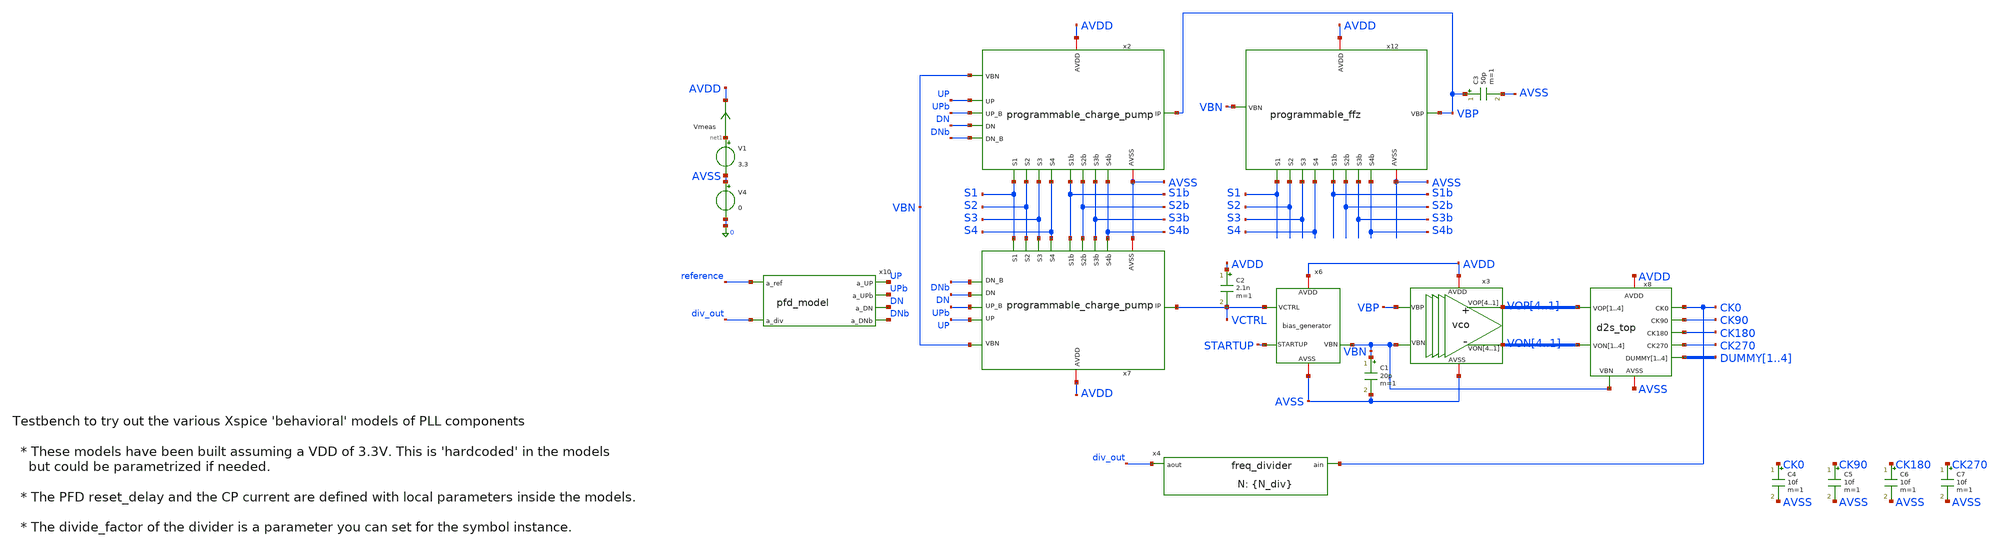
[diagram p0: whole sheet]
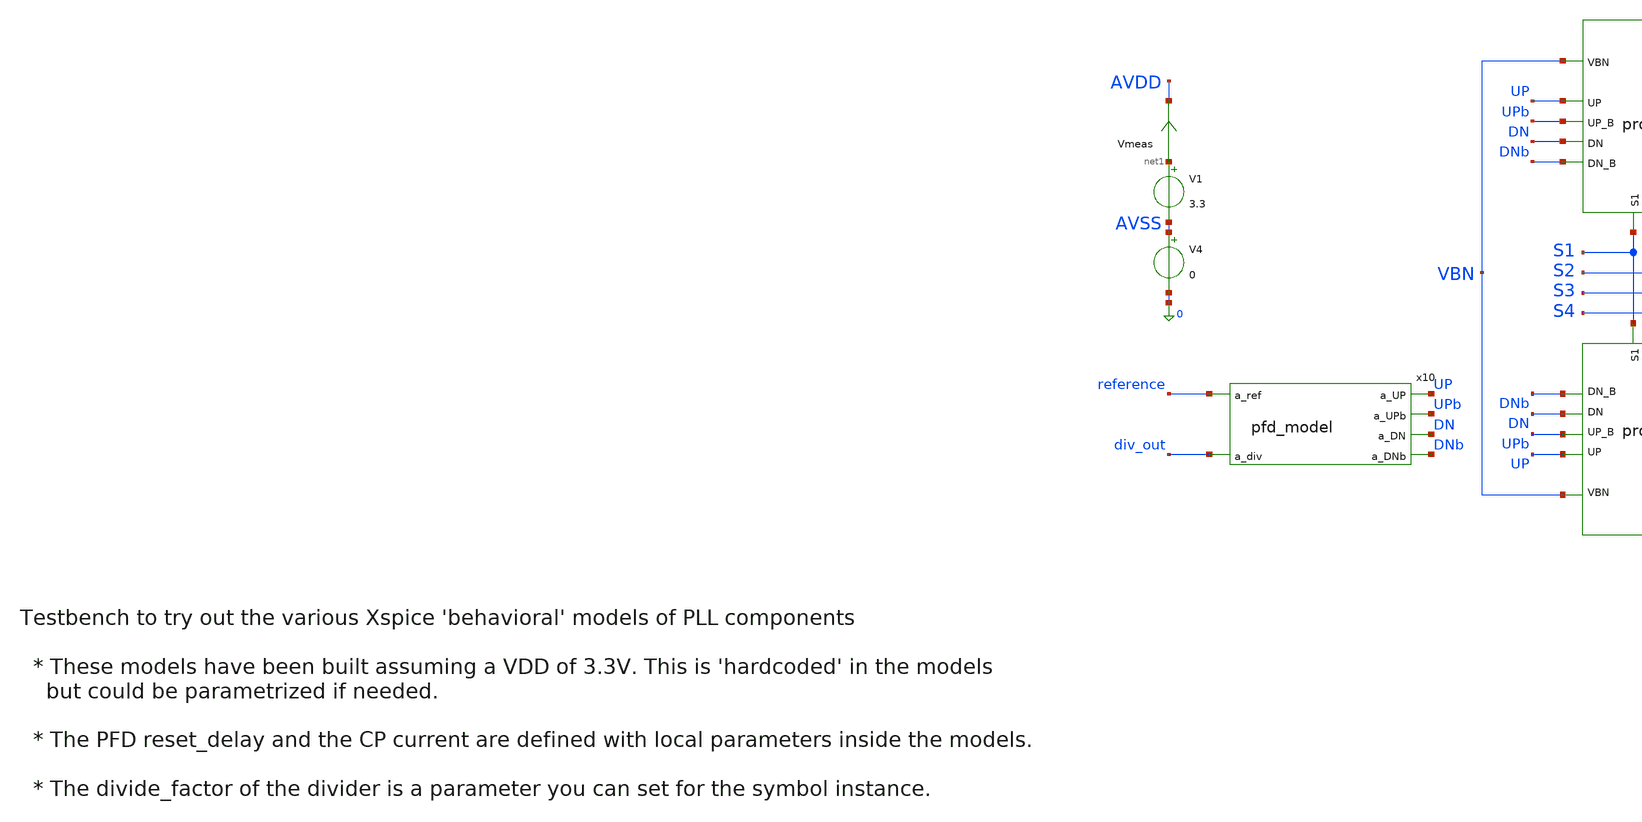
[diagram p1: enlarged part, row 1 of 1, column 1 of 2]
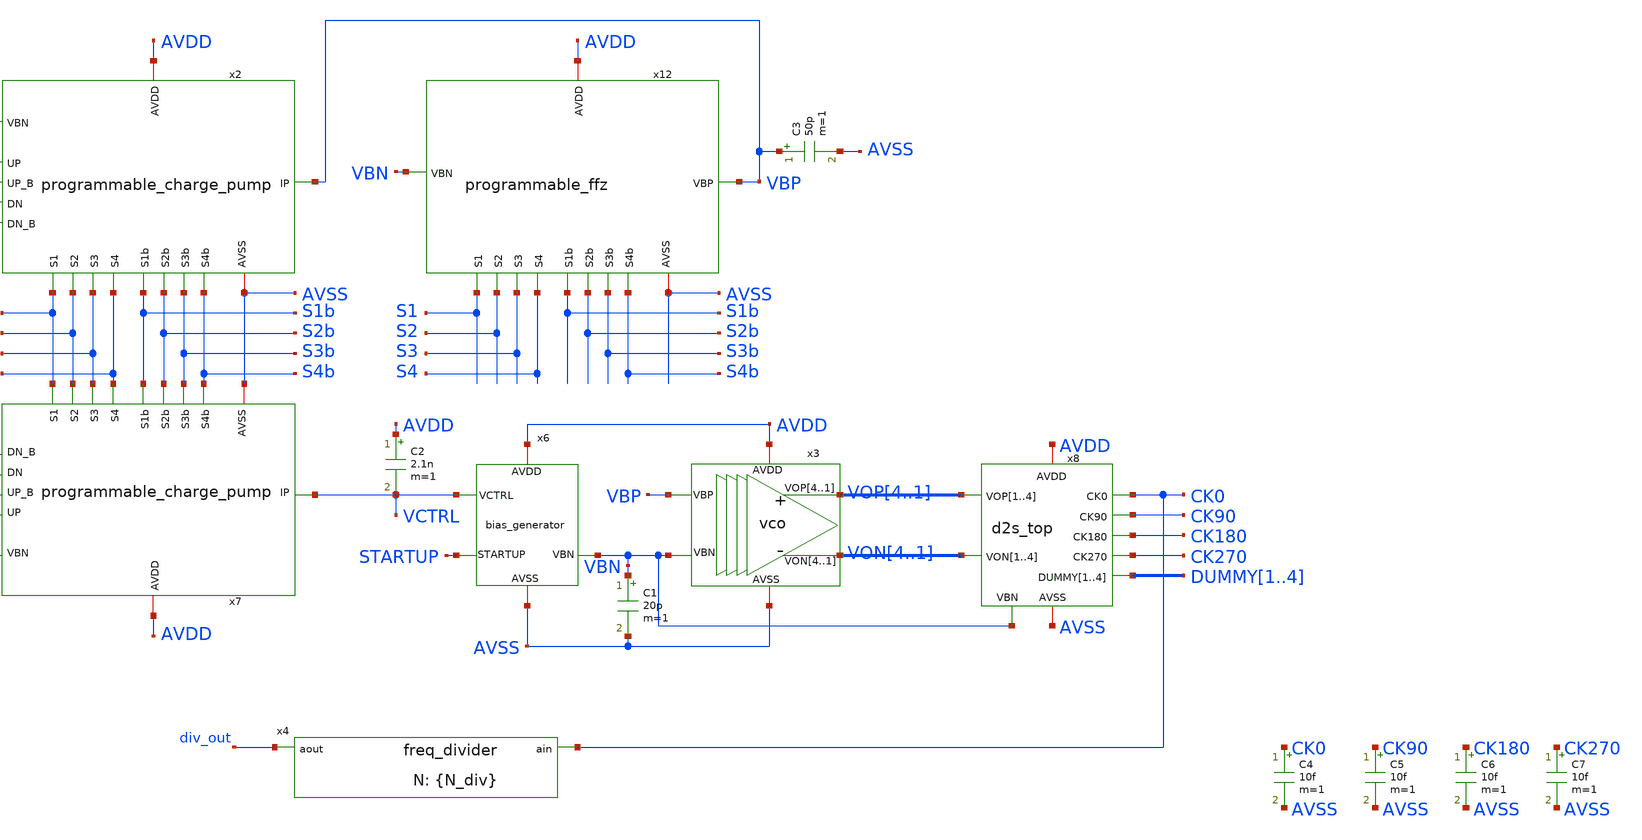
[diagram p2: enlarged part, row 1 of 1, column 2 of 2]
** sch_path: designs/libs/tb_pll/tb_PLL_CP_VCO_model.sch
**.subckt tb_PLL_CP_VCO_model
x4 div_out CK0 freq_divider divide_factor={N_div}
x3 VOP4 VOP3 VOP2 VOP1 VON4 VON3 VON2 VON1 AVDD AVSS VBP VBN vco
x6 VCTRL AVDD STARTUP AVSS VBN bias_generator
C2 AVDD VCTRL 2.1n m=1
V1 net1 AVSS 3.3
V4 AVSS 0 0
x2 AVSS AVDD UP UPb DN VBP DNb VBN S1b S1 S2b S2 S3b S3 S4b S4 programmable_charge_pump
x7 AVSS AVDD UP UPb DN VCTRL DNb VBN S1b S1 S2b S2 S3b S3 S4b S4 programmable_charge_pump
C1 VBN AVSS 20p m=1
C3 VBP AVSS 50p m=1
x12 VBP AVSS AVDD VBN S1b S1 S2b S2 S3b S3 S4b S4 programmable_ffz
x8 VOP4 VOP3 VOP2 VOP1 VON4 VON3 VON2 VON1 VBN DUMMY1 DUMMY2 DUMMY3 DUMMY4 CK0 CK90 CK180 CK270 AVDD
+ AVSS d2s_top
C4 CK0 AVSS 10f m=1
C5 CK90 AVSS 10f m=1
C6 CK180 AVSS 10f m=1
C7 CK270 AVSS 10f m=1
x10 reference UP UPb DN div_out DNb pfd_model
Vmeas net1 AVDD 0
.save i(vmeas)
**** begin user architecture code

.include $::180MCU_MODELS/design.ngspice
.lib $::180MCU_MODELS/sm141064.ngspice typical
*.lib $::180MCU_MODELS/sm141064.ngspice SS
*.lib $::180MCU_MODELS/sm141064.ngspice FF
*.lib $::180MCU_MODELS/sm141064.ngspice SF
*.lib $::180MCU_MODELS/sm141064.ngspice FS



==============Fref, N======================
.param f_ref=1MEG R_div=2 N_div=35

.ic v(VCTRL)=1.5 v(vbp)=1.5
==============Frequency Calculation========
.param tp_ref='td_ref/2' td_ref='1/f_ref'
Vref reference gnd pulse(0 3.3 0 10p 10p tp_ref td_ref)

.ic v(vop1)=3.3 v(von1)=0 v(startup)=0
.options reltol=1e-5 cshunt=1e-15 itl4=50 gmin=1e-12
.options method=gear

.param d1=0 d2=3.3 d3=3.3 d4=0
.param d1b=3.3 d2b=0 d3b=0 d4b=3.3

VS1 S1 0 d1
VS2 S2 0 d2
VS3 S3 0 d3
VS4 S4 0 d4

VS1b S1b 0 d1b
VS2b S2b 0 d2b
VS3b S3b 0 d3b
VS4b S4b 0 d4b

.control
set wr_singlescale
set wr_vecnames

save v(VCTRL) v(vbp) v(vbn) v(reference) v(div_out) v(pre_div) v(CK0) v(CK90) v(CK180) v(CK270)
+ v(up) v(dn)

tran 100p 15u

linearize v(CK0) v(CK90) v(CK180) v(CK270) v(VCTRL) v(vbp) v(vbn) v(reference) v(div_out) v(pre_div)
+ v(up) v(dn) i(vmeas)

meas tran I_vdd AVG i(vmeas) FROM=1u TO=15u

remzerovec

write tb2.raw
wrdata /foss/designs/synchronos-chipathon-2026/designs/libs/scripts/sim_data/tb2.txt tran.all

.endc


**** end user architecture code
**.ends
.end
